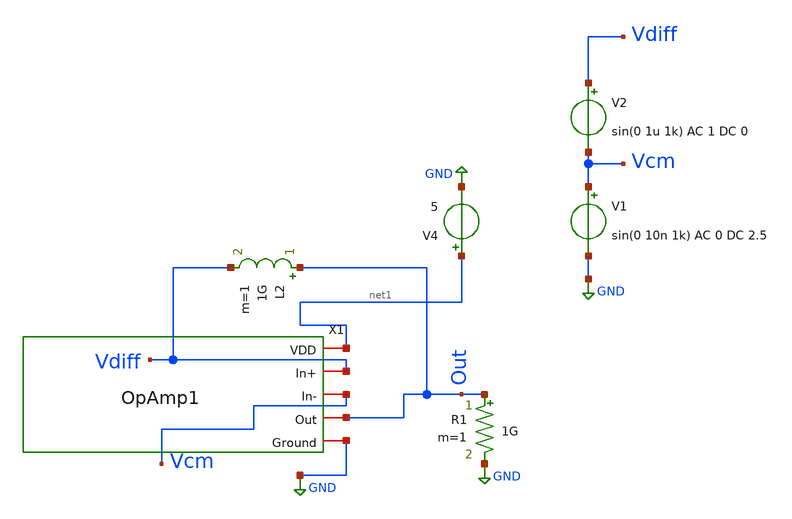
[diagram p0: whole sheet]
** sch_path: xschem/OpAmpTb.sch
**.subckt OpAmpTb
V1 Vcm GND sin(0 10n 1k) AC 0 DC 2.5
V2 Vdiff Vcm sin(0 1u 1k) AC 1 DC 0
V4 net1 GND 5
L2 Out Vdiff 1G m=1
R1 Out GND 1G m=1
X1 net1 Vdiff Vcm Out GND OpAmp1
**** begin user architecture code

** opencircuitdesign pdks install
.lib $::SKYWATER_MODELS/sky130.lib.spice tt



* this option enables mos model bin
* selection based on W/NF instead of W
.control
op
print all
save all
ac dec 10 1 1G
plot Vdb(Out)


.endc


**** end user architecture code
**.ends
.GLOBAL GND
.end
